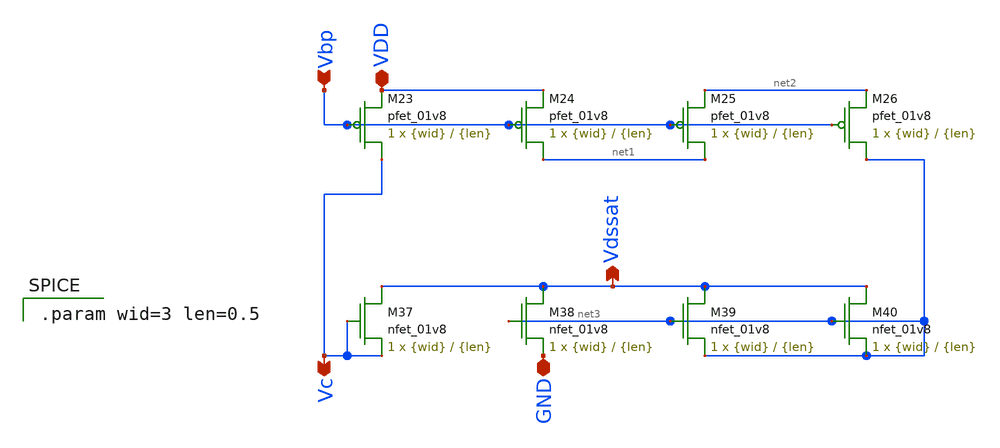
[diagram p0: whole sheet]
** sch_path: final/schematics/cascode_bias_lds.sch
**.subckt cascode_bias_lds GND Vc VDD Vbp Vdssat
*.iopin GND
*.opin Vc
*.iopin VDD
*.ipin Vbp
*.opin Vdssat
XM23 Vc Vbp VDD VDD sky130_fd_pr__pfet_01v8 L={len} W={wid} nf=1 ad='int((nf+1)/2) * W/nf * 0.29' as='int((nf+2)/2) * W/nf * 0.29'
+ pd='2*int((nf+1)/2) * (W/nf + 0.29)' ps='2*int((nf+2)/2) * (W/nf + 0.29)' nrd='0.29 / W' nrs='0.29 / W'
+ sa=0 sb=0 sd=0 mult=1 m=1
XM24 net1 Vbp VDD VDD sky130_fd_pr__pfet_01v8 L={len} W={wid} nf=1 ad='int((nf+1)/2) * W/nf * 0.29' as='int((nf+2)/2) * W/nf * 0.29'
+ pd='2*int((nf+1)/2) * (W/nf + 0.29)' ps='2*int((nf+2)/2) * (W/nf + 0.29)' nrd='0.29 / W' nrs='0.29 / W'
+ sa=0 sb=0 sd=0 mult=1 m=1
XM25 net1 Vbp net2 VDD sky130_fd_pr__pfet_01v8 L={len} W={wid} nf=1 ad='int((nf+1)/2) * W/nf * 0.29'
+ as='int((nf+2)/2) * W/nf * 0.29' pd='2*int((nf+1)/2) * (W/nf + 0.29)' ps='2*int((nf+2)/2) * (W/nf + 0.29)'
+ nrd='0.29 / W' nrs='0.29 / W' sa=0 sb=0 sd=0 mult=1 m=1
XM26 net3 Vbp net2 VDD sky130_fd_pr__pfet_01v8 L={len} W={wid} nf=1 ad='int((nf+1)/2) * W/nf * 0.29'
+ as='int((nf+2)/2) * W/nf * 0.29' pd='2*int((nf+1)/2) * (W/nf + 0.29)' ps='2*int((nf+2)/2) * (W/nf + 0.29)'
+ nrd='0.29 / W' nrs='0.29 / W' sa=0 sb=0 sd=0 mult=1 m=1
XM37 Vdssat Vc Vc GND sky130_fd_pr__nfet_01v8 L={len} W={wid} nf=1 ad='int((nf+1)/2) * W/nf * 0.29' as='int((nf+2)/2) * W/nf * 0.29'
+ pd='2*int((nf+1)/2) * (W/nf + 0.29)' ps='2*int((nf+2)/2) * (W/nf + 0.29)' nrd='0.29 / W' nrs='0.29 / W'
+ sa=0 sb=0 sd=0 mult=1 m=1
XM38 Vdssat net3 GND GND sky130_fd_pr__nfet_01v8 L={len} W={wid} nf=1 ad='int((nf+1)/2) * W/nf * 0.29'
+ as='int((nf+2)/2) * W/nf * 0.29' pd='2*int((nf+1)/2) * (W/nf + 0.29)' ps='2*int((nf+2)/2) * (W/nf + 0.29)'
+ nrd='0.29 / W' nrs='0.29 / W' sa=0 sb=0 sd=0 mult=1 m=1
XM39 Vdssat net3 net3 GND sky130_fd_pr__nfet_01v8 L={len} W={wid} nf=1 ad='int((nf+1)/2) * W/nf * 0.29'
+ as='int((nf+2)/2) * W/nf * 0.29' pd='2*int((nf+1)/2) * (W/nf + 0.29)' ps='2*int((nf+2)/2) * (W/nf + 0.29)'
+ nrd='0.29 / W' nrs='0.29 / W' sa=0 sb=0 sd=0 mult=1 m=1
XM40 Vdssat net3 net3 GND sky130_fd_pr__nfet_01v8 L={len} W={wid} nf=1 ad='int((nf+1)/2) * W/nf * 0.29'
+ as='int((nf+2)/2) * W/nf * 0.29' pd='2*int((nf+1)/2) * (W/nf + 0.29)' ps='2*int((nf+2)/2) * (W/nf + 0.29)'
+ nrd='0.29 / W' nrs='0.29 / W' sa=0 sb=0 sd=0 mult=1 m=1
**** begin user architecture code

.param wid=3 len=0.5

**** end user architecture code
**.ends
.end
